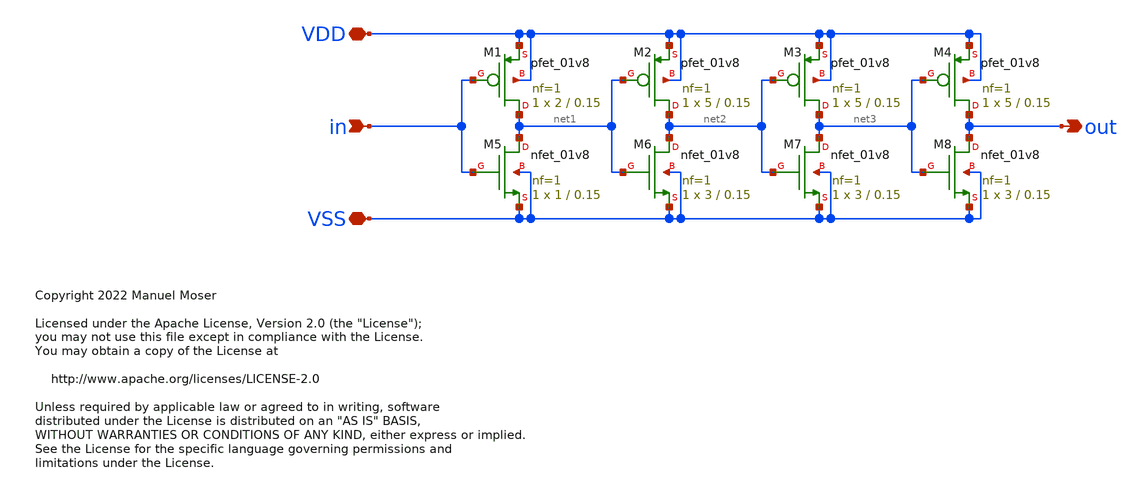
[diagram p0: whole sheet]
** sch_path: xschem/adc_sample_buffer/adc_sample_buffer.sch
* Copyright 2022 Manuel Moser
* Licensed under the Apache License, Version 2.0 (the "License");
**.subckt adc_sample_buffer in VDD VSS out
*.ipin in
*.iopin VDD
*.iopin VSS
*.opin out
XM1 net1 in VDD VDD sky130_fd_pr__pfet_01v8 L=0.15 W=2 nf=1 ad='int((nf+1)/2) * W/nf * 0.29' as='int((nf+2)/2) * W/nf * 0.29'
+ pd='2*int((nf+1)/2) * (W/nf + 0.29)' ps='2*int((nf+2)/2) * (W/nf + 0.29)' nrd='0.29 / W' nrs='0.29 / W'
+ sa=0 sb=0 sd=0 mult=1 m=1
XM2 net2 net1 VDD VDD sky130_fd_pr__pfet_01v8 L=0.15 W=5 nf=1 ad='int((nf+1)/2) * W/nf * 0.29' as='int((nf+2)/2) * W/nf * 0.29'
+ pd='2*int((nf+1)/2) * (W/nf + 0.29)' ps='2*int((nf+2)/2) * (W/nf + 0.29)' nrd='0.29 / W' nrs='0.29 / W'
+ sa=0 sb=0 sd=0 mult=1 m=1
XM3 net3 net2 VDD VDD sky130_fd_pr__pfet_01v8 L=0.15 W=5 nf=1 ad='int((nf+1)/2) * W/nf * 0.29' as='int((nf+2)/2) * W/nf * 0.29'
+ pd='2*int((nf+1)/2) * (W/nf + 0.29)' ps='2*int((nf+2)/2) * (W/nf + 0.29)' nrd='0.29 / W' nrs='0.29 / W'
+ sa=0 sb=0 sd=0 mult=1 m=1
XM4 out net3 VDD VDD sky130_fd_pr__pfet_01v8 L=0.15 W=5 nf=1 ad='int((nf+1)/2) * W/nf * 0.29' as='int((nf+2)/2) * W/nf * 0.29'
+ pd='2*int((nf+1)/2) * (W/nf + 0.29)' ps='2*int((nf+2)/2) * (W/nf + 0.29)' nrd='0.29 / W' nrs='0.29 / W'
+ sa=0 sb=0 sd=0 mult=1 m=1
XM5 net1 in VSS VSS sky130_fd_pr__nfet_01v8 L=0.15 W=1 nf=1 ad='int((nf+1)/2) * W/nf * 0.29' as='int((nf+2)/2) * W/nf * 0.29'
+ pd='2*int((nf+1)/2) * (W/nf + 0.29)' ps='2*int((nf+2)/2) * (W/nf + 0.29)' nrd='0.29 / W' nrs='0.29 / W'
+ sa=0 sb=0 sd=0 mult=1 m=1
XM6 net2 net1 VSS VSS sky130_fd_pr__nfet_01v8 L=0.15 W=3 nf=1 ad='int((nf+1)/2) * W/nf * 0.29' as='int((nf+2)/2) * W/nf * 0.29'
+ pd='2*int((nf+1)/2) * (W/nf + 0.29)' ps='2*int((nf+2)/2) * (W/nf + 0.29)' nrd='0.29 / W' nrs='0.29 / W'
+ sa=0 sb=0 sd=0 mult=1 m=1
XM7 net3 net2 VSS VSS sky130_fd_pr__nfet_01v8 L=0.15 W=3 nf=1 ad='int((nf+1)/2) * W/nf * 0.29' as='int((nf+2)/2) * W/nf * 0.29'
+ pd='2*int((nf+1)/2) * (W/nf + 0.29)' ps='2*int((nf+2)/2) * (W/nf + 0.29)' nrd='0.29 / W' nrs='0.29 / W'
+ sa=0 sb=0 sd=0 mult=1 m=1
XM8 out net3 VSS VSS sky130_fd_pr__nfet_01v8 L=0.15 W=3 nf=1 ad='int((nf+1)/2) * W/nf * 0.29' as='int((nf+2)/2) * W/nf * 0.29'
+ pd='2*int((nf+1)/2) * (W/nf + 0.29)' ps='2*int((nf+2)/2) * (W/nf + 0.29)' nrd='0.29 / W' nrs='0.29 / W'
+ sa=0 sb=0 sd=0 mult=1 m=1
**.ends
.end
